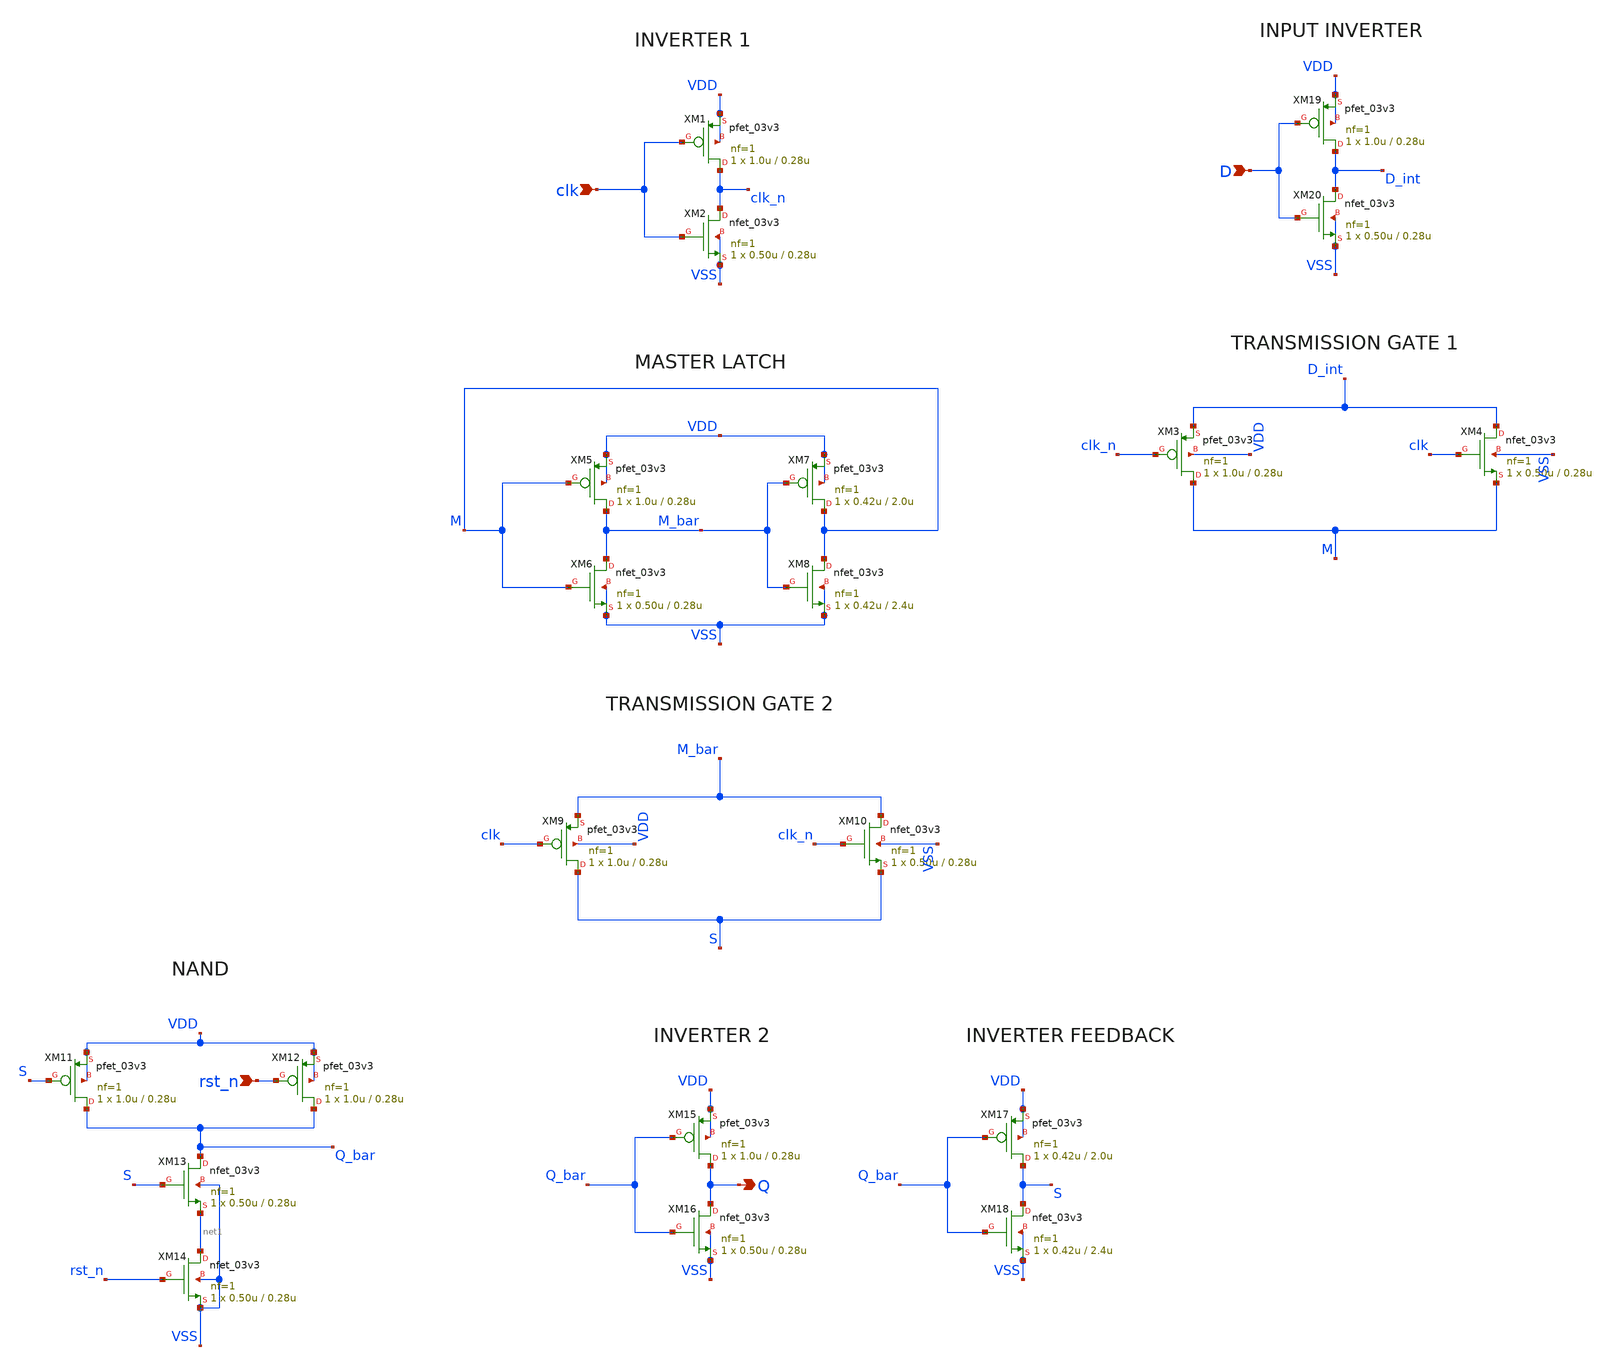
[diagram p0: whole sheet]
** sch_path: xschem/sar_adc/blocks/async_sar/dff_cell.sch
**.subckt dff_cell D clk rst_n Q
*.ipin D
*.ipin clk
*.ipin rst_n
*.opin Q
XM1 clk_n clk VDD VDD pfet_03v3 L=0.28u W=1.0u nf=1 ad='int((nf+1)/2) * W/nf * 0.18u' as='int((nf+2)/2) * W/nf * 0.18u'
+ pd='2*int((nf+1)/2) * (W/nf + 0.18u)' ps='2*int((nf+2)/2) * (W/nf + 0.18u)' nrd='0.18u / W' nrs='0.18u / W'
+ sa=0 sb=0 sd=0 m=1
XM2 clk_n clk VSS VSS nfet_03v3 L=0.28u W=0.50u nf=1 ad='int((nf+1)/2) * W/nf * 0.18u' as='int((nf+2)/2) * W/nf * 0.18u'
+ pd='2*int((nf+1)/2) * (W/nf + 0.18u)' ps='2*int((nf+2)/2) * (W/nf + 0.18u)' nrd='0.18u / W' nrs='0.18u / W'
+ sa=0 sb=0 sd=0 m=1
XM3 M clk_n D_int VDD pfet_03v3 L=0.28u W=1.0u nf=1 ad='int((nf+1)/2) * W/nf * 0.18u' as='int((nf+2)/2) * W/nf * 0.18u'
+ pd='2*int((nf+1)/2) * (W/nf + 0.18u)' ps='2*int((nf+2)/2) * (W/nf + 0.18u)' nrd='0.18u / W' nrs='0.18u / W'
+ sa=0 sb=0 sd=0 m=1
XM4 D_int clk M VSS nfet_03v3 L=0.28u W=0.50u nf=1 ad='int((nf+1)/2) * W/nf * 0.18u' as='int((nf+2)/2) * W/nf * 0.18u'
+ pd='2*int((nf+1)/2) * (W/nf + 0.18u)' ps='2*int((nf+2)/2) * (W/nf + 0.18u)' nrd='0.18u / W' nrs='0.18u / W'
+ sa=0 sb=0 sd=0 m=1
XM5 M_bar M VDD VDD pfet_03v3 L=0.28u W=1.0u nf=1 ad='int((nf+1)/2) * W/nf * 0.18u' as='int((nf+2)/2) * W/nf * 0.18u'
+ pd='2*int((nf+1)/2) * (W/nf + 0.18u)' ps='2*int((nf+2)/2) * (W/nf + 0.18u)' nrd='0.18u / W' nrs='0.18u / W'
+ sa=0 sb=0 sd=0 m=1
XM6 M_bar M VSS VSS nfet_03v3 L=0.28u W=0.50u nf=1 ad='int((nf+1)/2) * W/nf * 0.18u' as='int((nf+2)/2) * W/nf * 0.18u'
+ pd='2*int((nf+1)/2) * (W/nf + 0.18u)' ps='2*int((nf+2)/2) * (W/nf + 0.18u)' nrd='0.18u / W' nrs='0.18u / W'
+ sa=0 sb=0 sd=0 m=1
XM7 M M_bar VDD VDD pfet_03v3 L=2.0u W=0.42u nf=1 ad='int((nf+1)/2) * W/nf * 0.18u' as='int((nf+2)/2) * W/nf * 0.18u'
+ pd='2*int((nf+1)/2) * (W/nf + 0.18u)' ps='2*int((nf+2)/2) * (W/nf + 0.18u)' nrd='0.18u / W' nrs='0.18u / W'
+ sa=0 sb=0 sd=0 m=1
XM8 M M_bar VSS VSS nfet_03v3 L=2.4u W=0.42u nf=1 ad='int((nf+1)/2) * W/nf * 0.18u' as='int((nf+2)/2) * W/nf * 0.18u'
+ pd='2*int((nf+1)/2) * (W/nf + 0.18u)' ps='2*int((nf+2)/2) * (W/nf + 0.18u)' nrd='0.18u / W' nrs='0.18u / W'
+ sa=0 sb=0 sd=0 m=1
XM9 S clk M_bar VDD pfet_03v3 L=0.28u W=1.0u nf=1 ad='int((nf+1)/2) * W/nf * 0.18u' as='int((nf+2)/2) * W/nf * 0.18u'
+ pd='2*int((nf+1)/2) * (W/nf + 0.18u)' ps='2*int((nf+2)/2) * (W/nf + 0.18u)' nrd='0.18u / W' nrs='0.18u / W'
+ sa=0 sb=0 sd=0 m=1
XM10 M_bar clk_n S VSS nfet_03v3 L=0.28u W=0.50u nf=1 ad='int((nf+1)/2) * W/nf * 0.18u' as='int((nf+2)/2) * W/nf * 0.18u'
+ pd='2*int((nf+1)/2) * (W/nf + 0.18u)' ps='2*int((nf+2)/2) * (W/nf + 0.18u)' nrd='0.18u / W' nrs='0.18u / W'
+ sa=0 sb=0 sd=0 m=1
XM11 Q_bar S VDD VDD pfet_03v3 L=0.28u W=1.0u nf=1 ad='int((nf+1)/2) * W/nf * 0.18u' as='int((nf+2)/2) * W/nf * 0.18u'
+ pd='2*int((nf+1)/2) * (W/nf + 0.18u)' ps='2*int((nf+2)/2) * (W/nf + 0.18u)' nrd='0.18u / W' nrs='0.18u / W'
+ sa=0 sb=0 sd=0 m=1
XM12 Q_bar rst_n VDD VDD pfet_03v3 L=0.28u W=1.0u nf=1 ad='int((nf+1)/2) * W/nf * 0.18u' as='int((nf+2)/2) * W/nf * 0.18u'
+ pd='2*int((nf+1)/2) * (W/nf + 0.18u)' ps='2*int((nf+2)/2) * (W/nf + 0.18u)' nrd='0.18u / W' nrs='0.18u / W'
+ sa=0 sb=0 sd=0 m=1
XM13 Q_bar S net1 VSS nfet_03v3 L=0.28u W=0.50u nf=1 ad='int((nf+1)/2) * W/nf * 0.18u' as='int((nf+2)/2) * W/nf * 0.18u'
+ pd='2*int((nf+1)/2) * (W/nf + 0.18u)' ps='2*int((nf+2)/2) * (W/nf + 0.18u)' nrd='0.18u / W' nrs='0.18u / W'
+ sa=0 sb=0 sd=0 m=1
XM14 net1 rst_n VSS VSS nfet_03v3 L=0.28u W=0.50u nf=1 ad='int((nf+1)/2) * W/nf * 0.18u' as='int((nf+2)/2) * W/nf * 0.18u'
+ pd='2*int((nf+1)/2) * (W/nf + 0.18u)' ps='2*int((nf+2)/2) * (W/nf + 0.18u)' nrd='0.18u / W' nrs='0.18u / W'
+ sa=0 sb=0 sd=0 m=1
XM15 Q Q_bar VDD VDD pfet_03v3 L=0.28u W=1.0u nf=1 ad='int((nf+1)/2) * W/nf * 0.18u' as='int((nf+2)/2) * W/nf * 0.18u'
+ pd='2*int((nf+1)/2) * (W/nf + 0.18u)' ps='2*int((nf+2)/2) * (W/nf + 0.18u)' nrd='0.18u / W' nrs='0.18u / W'
+ sa=0 sb=0 sd=0 m=1
XM16 Q Q_bar VSS VSS nfet_03v3 L=0.28u W=0.50u nf=1 ad='int((nf+1)/2) * W/nf * 0.18u' as='int((nf+2)/2) * W/nf * 0.18u'
+ pd='2*int((nf+1)/2) * (W/nf + 0.18u)' ps='2*int((nf+2)/2) * (W/nf + 0.18u)' nrd='0.18u / W' nrs='0.18u / W'
+ sa=0 sb=0 sd=0 m=1
XM17 S Q_bar VDD VDD pfet_03v3 L=2.0u W=0.42u nf=1 ad='int((nf+1)/2) * W/nf * 0.18u' as='int((nf+2)/2) * W/nf * 0.18u'
+ pd='2*int((nf+1)/2) * (W/nf + 0.18u)' ps='2*int((nf+2)/2) * (W/nf + 0.18u)' nrd='0.18u / W' nrs='0.18u / W'
+ sa=0 sb=0 sd=0 m=1
XM18 S Q_bar VSS VSS nfet_03v3 L=2.4u W=0.42u nf=1 ad='int((nf+1)/2) * W/nf * 0.18u' as='int((nf+2)/2) * W/nf * 0.18u'
+ pd='2*int((nf+1)/2) * (W/nf + 0.18u)' ps='2*int((nf+2)/2) * (W/nf + 0.18u)' nrd='0.18u / W' nrs='0.18u / W'
+ sa=0 sb=0 sd=0 m=1
XM19 D_int D VDD VDD pfet_03v3 L=0.28u W=1.0u nf=1 ad='int((nf+1)/2) * W/nf * 0.18u' as='int((nf+2)/2) * W/nf * 0.18u'
+ pd='2*int((nf+1)/2) * (W/nf + 0.18u)' ps='2*int((nf+2)/2) * (W/nf + 0.18u)' nrd='0.18u / W' nrs='0.18u / W'
+ sa=0 sb=0 sd=0 m=1
XM20 D_int D VSS VSS nfet_03v3 L=0.28u W=0.50u nf=1 ad='int((nf+1)/2) * W/nf * 0.18u' as='int((nf+2)/2) * W/nf * 0.18u'
+ pd='2*int((nf+1)/2) * (W/nf + 0.18u)' ps='2*int((nf+2)/2) * (W/nf + 0.18u)' nrd='0.18u / W' nrs='0.18u / W'
+ sa=0 sb=0 sd=0 m=1
**.ends
.end
